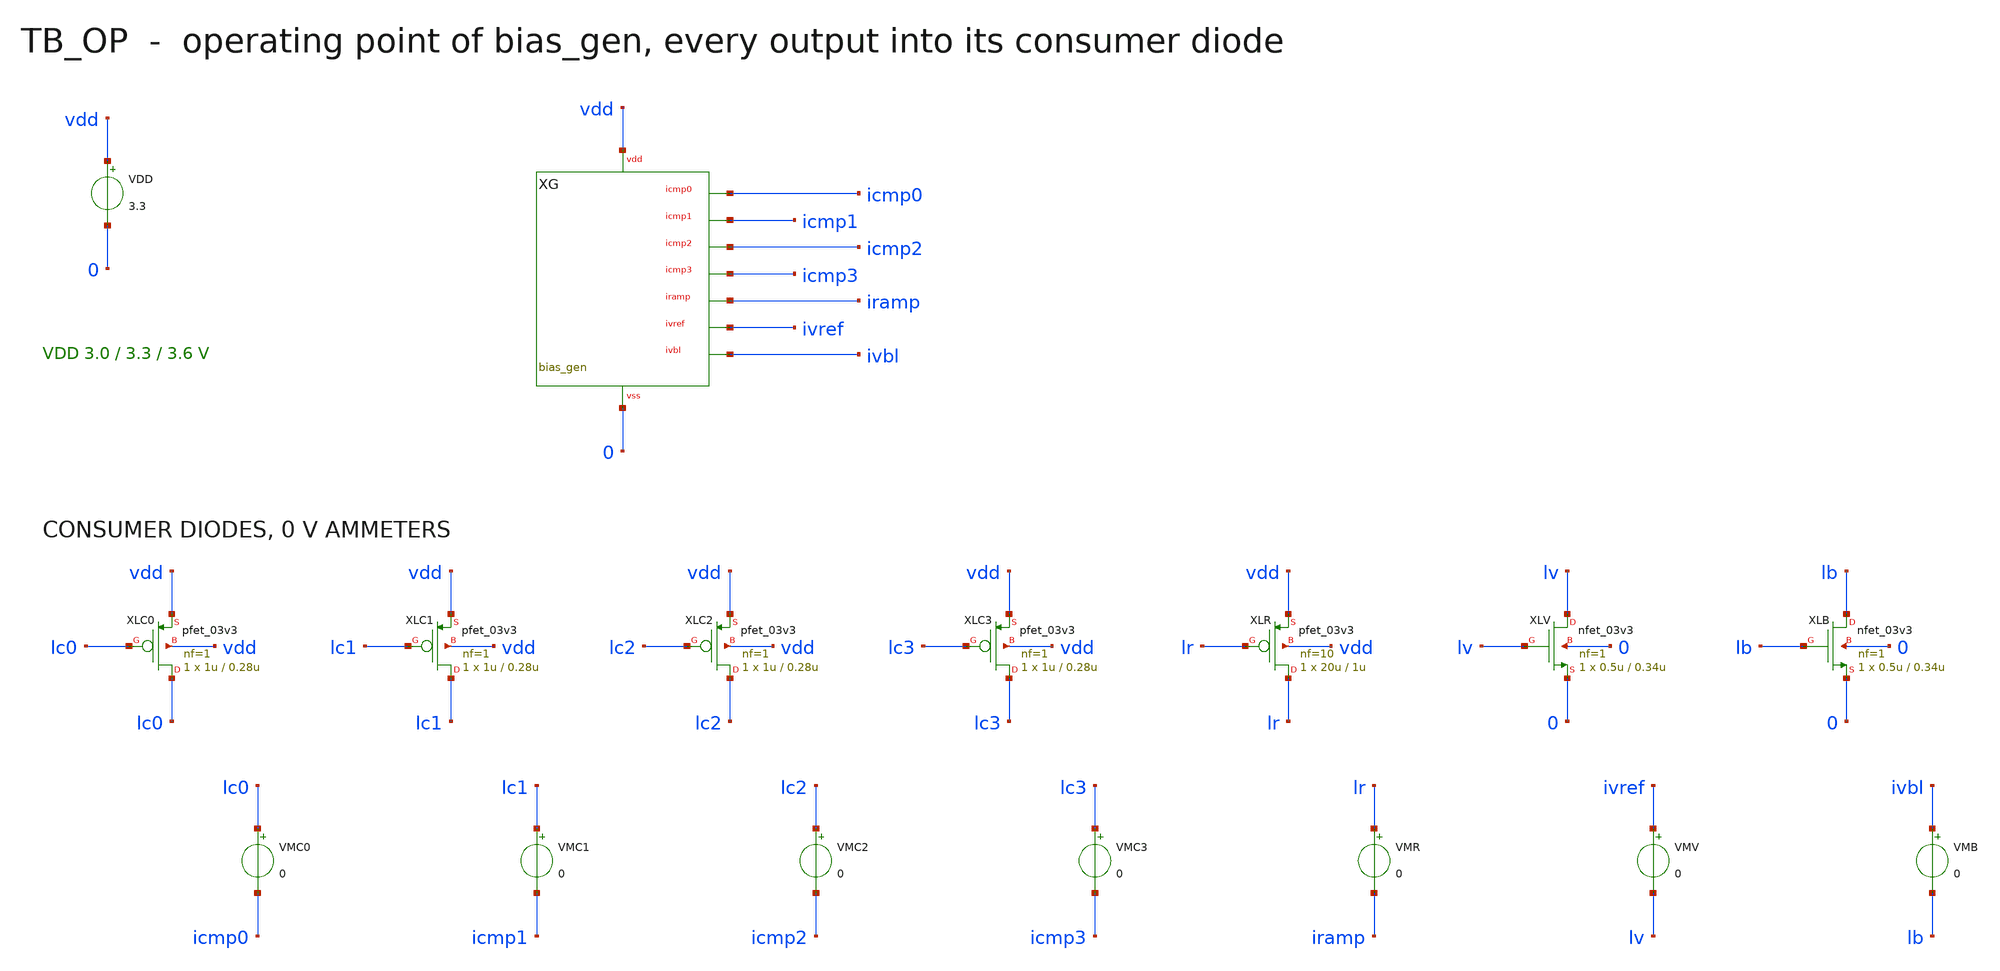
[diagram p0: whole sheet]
** sch_path: mixed_signal/bias_gen/tb_op.sch
**.subckt tb_op
VDD vdd 0 3.3
XG vdd 0 icmp0 icmp1 icmp2 icmp3 iramp ivref ivbl bias_gen
XLC0 lc0 lc0 vdd vdd pfet_03v3 L=0.28u W=1u nf=1 m=1 ad=0.18p pd=2.36u as=0.18p ps=2.36u nrd=0.18
+ nrs=0.18
VMC0 lc0 icmp0 0
XLC1 lc1 lc1 vdd vdd pfet_03v3 L=0.28u W=1u nf=1 m=1 ad=0.18p pd=2.36u as=0.18p ps=2.36u nrd=0.18
+ nrs=0.18
VMC1 lc1 icmp1 0
XLC2 lc2 lc2 vdd vdd pfet_03v3 L=0.28u W=1u nf=1 m=1 ad=0.18p pd=2.36u as=0.18p ps=2.36u nrd=0.18
+ nrs=0.18
VMC2 lc2 icmp2 0
XLC3 lc3 lc3 vdd vdd pfet_03v3 L=0.28u W=1u nf=1 m=1 ad=0.18p pd=2.36u as=0.18p ps=2.36u nrd=0.18
+ nrs=0.18
VMC3 lc3 icmp3 0
XLR lr lr vdd vdd pfet_03v3 L=1u W=20u nf=10 m=1 ad=1.8p pd=21.8u as=2.16p ps=26.16u nrd=0.009
+ nrs=0.009
VMR lr iramp 0
XLV lv lv 0 0 nfet_03v3 L=0.34u W=0.5u nf=1 m=1 ad=0.09p pd=1.36u as=0.09p ps=1.36u nrd=0.36
+ nrs=0.36
VMV ivref lv 0
XLB lb lb 0 0 nfet_03v3 L=0.34u W=0.5u nf=1 m=1 ad=0.09p pd=1.36u as=0.09p ps=1.36u nrd=0.36
+ nrs=0.36
VMB ivbl lb 0
**** begin user architecture code

.include /foss/pdks/gf180mcuD/libs.tech/ngspice/design.ngspice
.lib /foss/pdks/gf180mcuD/libs.tech/ngspice/sm141064.ngspice typical
.lib /foss/pdks/gf180mcuD/libs.tech/ngspice/sm141064.ngspice res_typical
.lib /foss/pdks/gf180mcuD/libs.tech/ngspice/sm141064.ngspice mimcap_typical
.temp 27
.control
set num_threads=1
foreach v 3 3.3 3.6
alter VDD dc = $v
op
let ic = abs(i(vmc0))
let ic1 = abs(i(vmc1))
let ir = abs(i(vmr))
let iv = abs(i(vmv))
let icore = abs(@m.xg.xmn1.m0[id])
let ibl = abs(@m.xg.xsu4.m0[id])
let isup = -i(vdd)
let vsu = v(xg.su)
let vnb = v(xg.nb)
let vpb = v(xg.pb)
let vlc = v(lc0)
let vlr = v(lr)
let vlv = v(lv)
let hr_xmn1 = abs(@m.xg.xmn1.m0[vds]) - abs(@m.xg.xmn1.m0[vdsat])
let hr_xmn2 = abs(@m.xg.xmn2.m0[vds]) - abs(@m.xg.xmn2.m0[vdsat])
let hr_xmp1 = abs(@m.xg.xmp1.m0[vds]) - abs(@m.xg.xmp1.m0[vdsat])
let hr_xmp2 = abs(@m.xg.xmp2.m0[vds]) - abs(@m.xg.xmp2.m0[vdsat])
let hr_xoc0 = abs(@m.xg.xoc0.m0[vds]) - abs(@m.xg.xoc0.m0[vdsat])
let hr_xoc1 = abs(@m.xg.xoc1.m0[vds]) - abs(@m.xg.xoc1.m0[vdsat])
let hr_xoc2 = abs(@m.xg.xoc2.m0[vds]) - abs(@m.xg.xoc2.m0[vdsat])
let hr_xoc3 = abs(@m.xg.xoc3.m0[vds]) - abs(@m.xg.xoc3.m0[vdsat])
let hr_xor = abs(@m.xg.xor.m0[vds]) - abs(@m.xg.xor.m0[vdsat])
let hr_xov = abs(@m.xg.xov.m0[vds]) - abs(@m.xg.xov.m0[vdsat])
let hr_xob = abs(@m.xg.xob.m0[vds]) - abs(@m.xg.xob.m0[vdsat])
echo OP typical 27 res_typical $v $&ic $&ic1 $&ir $&iv $&icore $&ibl $&isup $&vsu $&vnb $&vpb $&vlc
+ $&vlr $&vlv $&hr_xmn1 $&hr_xmn2 $&hr_xmp1 $&hr_xmp2 $&hr_xoc0 $&hr_xoc1 $&hr_xoc2 $&hr_xoc3 $&hr_xor
+ $&hr_xov $&hr_xob
end
quit
.endc

**** end user architecture code
**.ends
.end
